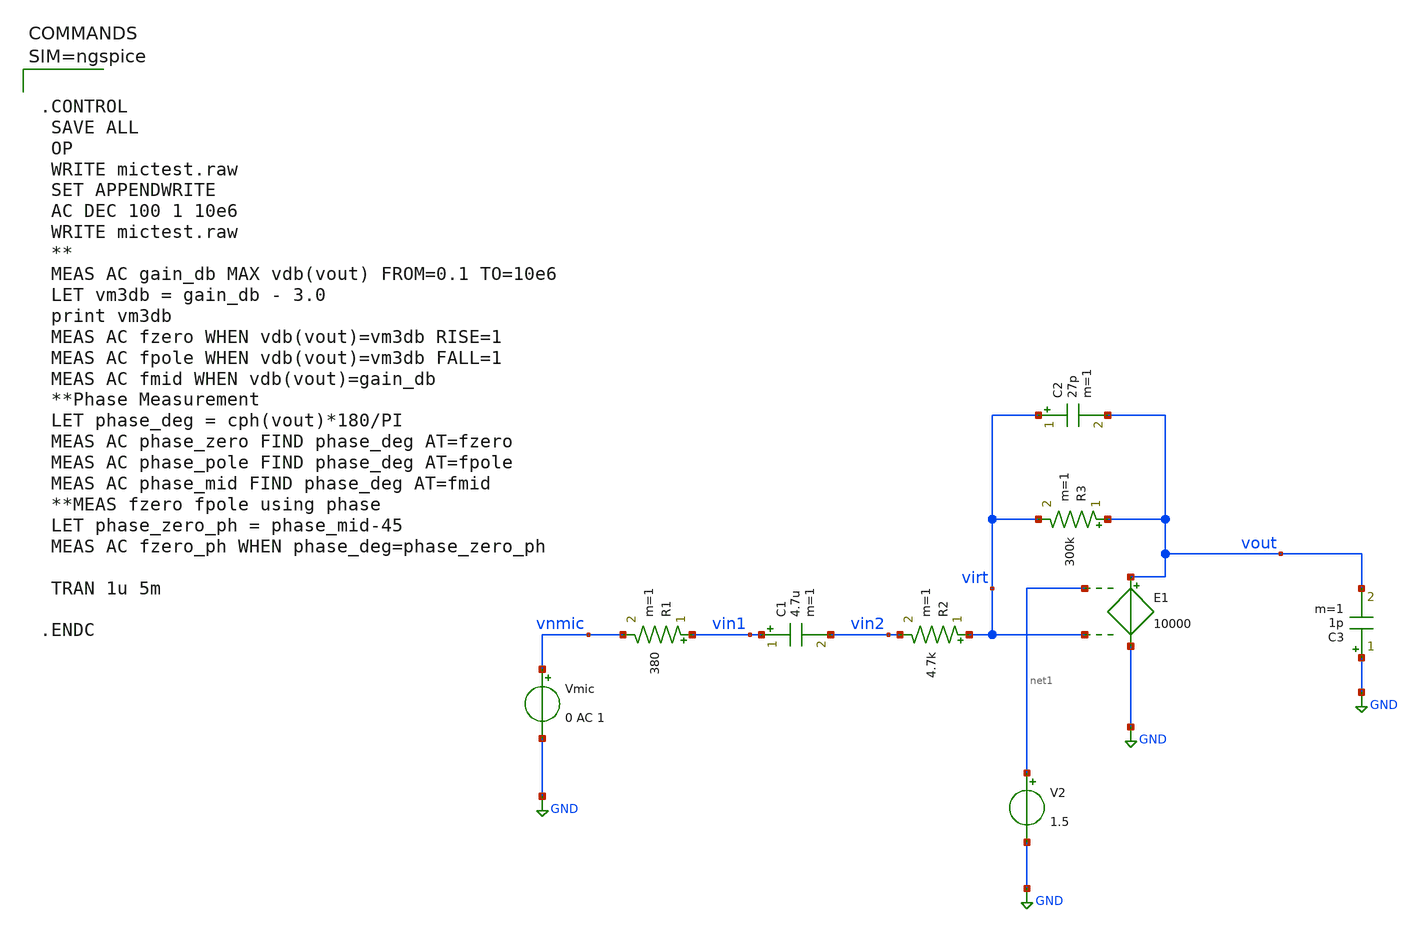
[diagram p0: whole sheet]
** sch_path: xschem/mictest_op2.sch
**.subckt mictest_op2
Vmic vnmic GND 0 AC 1
R1 vin1 vnmic 380 m=1
C1 vin1 vin2 4.7u m=1
R2 virt vin2 4.7k m=1
R3 vout virt 300k m=1
C2 virt vout 27p m=1
V2 net1 GND 1.5
C3 GND vout 1p m=1
E1 vout GND net1 virt 10000
**** begin user architecture code



.CONTROL
 SAVE ALL
 OP
 WRITE mictest.raw
 SET APPENDWRITE
 AC DEC 100 1 10e6
 WRITE mictest.raw
 **
 MEAS AC gain_db MAX vdb(vout) FROM=0.1 TO=10e6
 LET vm3db = gain_db - 3.0
 print vm3db
 MEAS AC fzero WHEN vdb(vout)=vm3db RISE=1
 MEAS AC fpole WHEN vdb(vout)=vm3db FALL=1
 MEAS AC fmid WHEN vdb(vout)=gain_db
 **Phase Measurement
 LET phase_deg = cph(vout)*180/PI
 MEAS AC phase_zero FIND phase_deg AT=fzero
 MEAS AC phase_pole FIND phase_deg AT=fpole
 MEAS AC phase_mid FIND phase_deg AT=fmid
 **MEAS fzero fpole using phase
 LET phase_zero_ph = phase_mid-45
 MEAS AC fzero_ph WHEN phase_deg=phase_zero_ph

 TRAN 1u 5m

.ENDC



**** end user architecture code
**.ends
.GLOBAL GND
.end
